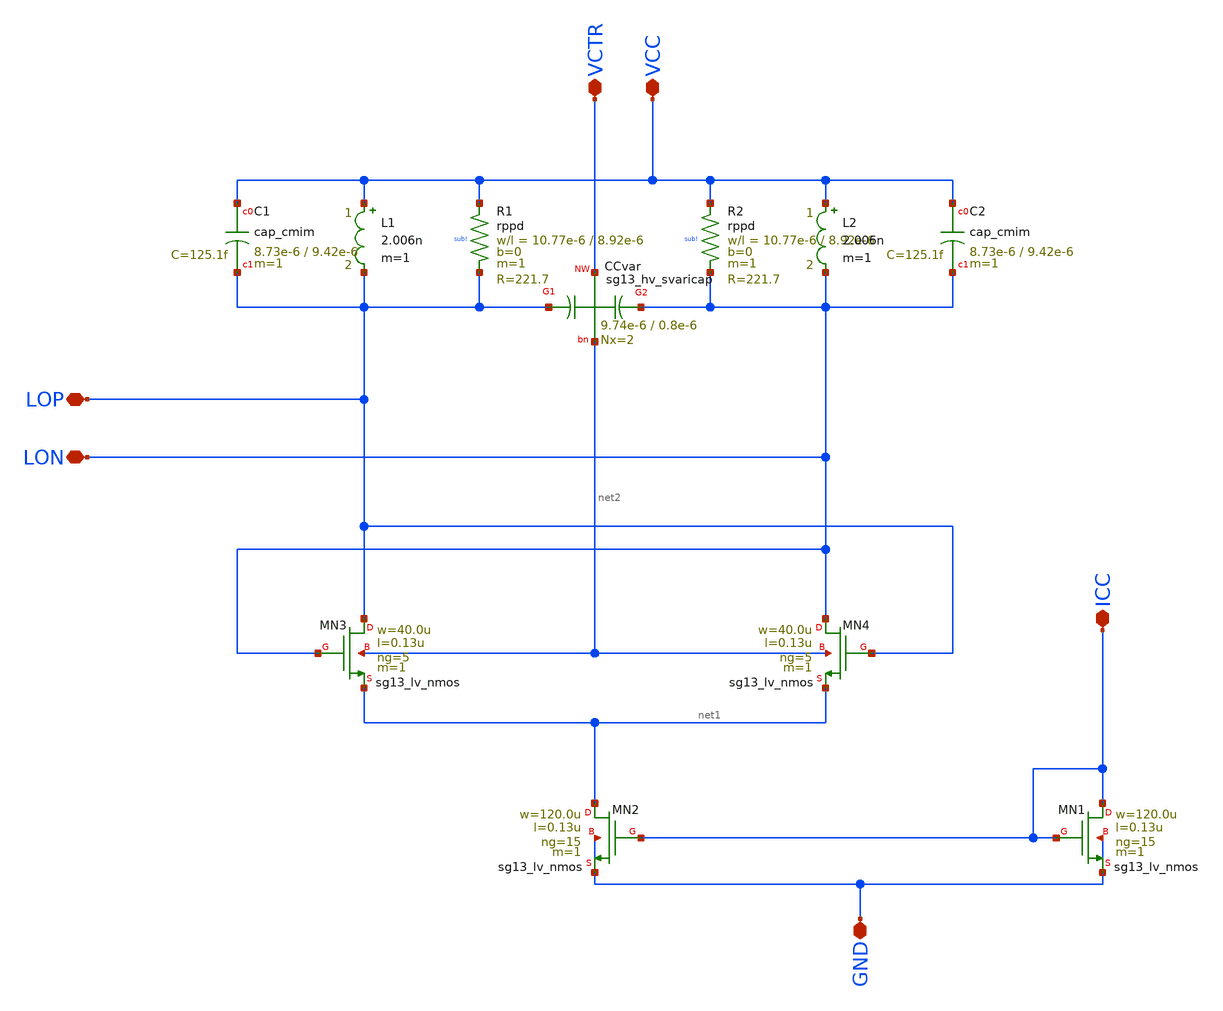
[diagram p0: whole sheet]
** sch_path: xschem/LC_VCO.sch
**.subckt LC_VCO LON LOP VCC ICC GND VCTR
*.iopin LON
*.iopin LOP
*.iopin VCC
*.iopin ICC
*.iopin GND
*.iopin VCTR
XMN3 LOP LON net1 net2 sg13_lv_nmos w=40.0u l=0.13u ng=5 m=1 mm_ok=1
XMN4 LON LOP net1 net2 sg13_lv_nmos w=40.0u l=0.13u ng=5 m=1 mm_ok=1
XMN1 ICC ICC GND GND sg13_lv_nmos w=120.0u l=0.13u ng=15 m=1 mm_ok=1
XMN2 net1 ICC GND GND sg13_lv_nmos w=120.0u l=0.13u ng=15 m=1 mm_ok=1
XC1 VCC LOP cap_cmim w=8.73e-6 l=9.42e-6 m=1 mm_ok=1
XR1 VCC LOP sub! rppd w=10.77e-6 l=8.92e-6 m=1 b=0 mm_ok=1
XC2 VCC LON cap_cmim w=8.73e-6 l=9.42e-6 m=1 mm_ok=1
XR2 VCC LON sub! rppd w=10.77e-6 l=8.92e-6 m=1 b=0 mm_ok=1
L1 VCC LOP 2.006n m=1
L2 VCC LON 2.006n m=1
XCvar LOP VCTR LON net2 sg13_hv_svaricap w=9.74e-6 l=0.8e-6 Nx=2
**.ends
.end
